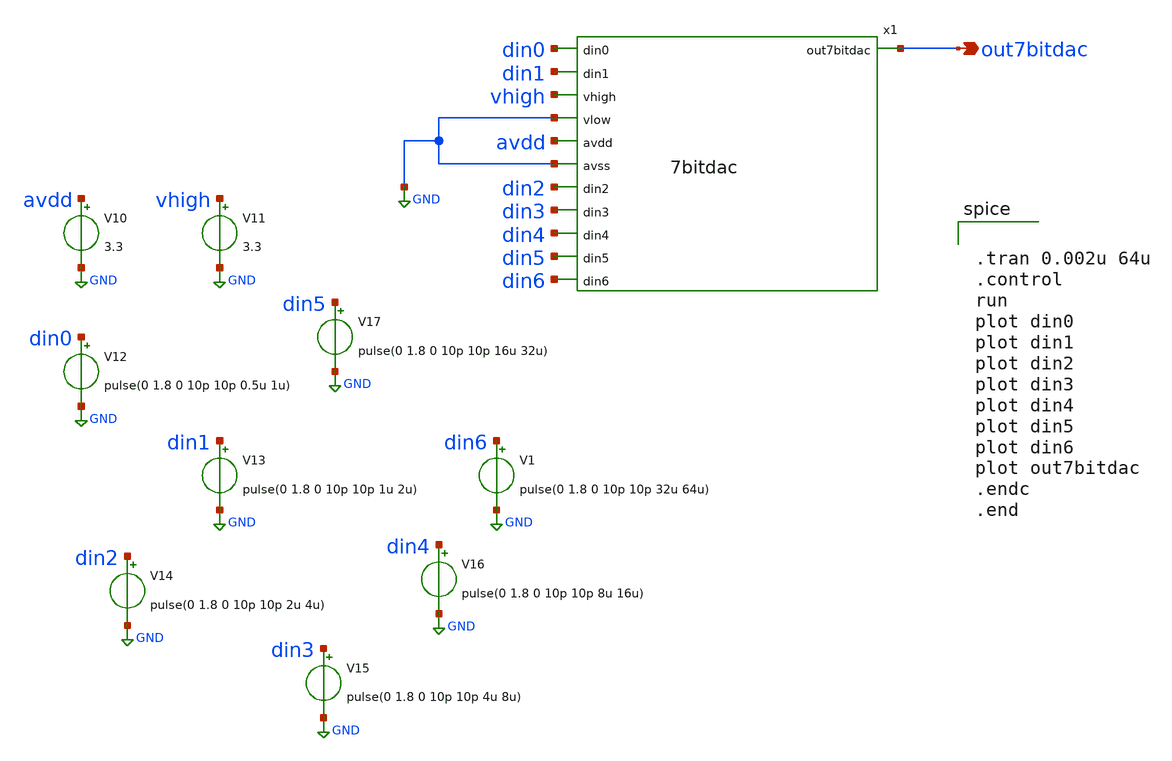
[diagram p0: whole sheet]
** sch_path: xschem/tb_7bitdac.sch
**.subckt tb_7bitdac out7bitdac
*.opin out7bitdac
x1 out7bitdac din0 din1 vhigh GND avdd GND din2 din3 din4 din5 din6 7bitdac
V10 avdd GND 3.3
V11 vhigh GND 3.3
V12 din0 GND pulse(0 1.8 0 10p 10p 0.5u 1u)
V13 din1 GND pulse(0 1.8 0 10p 10p 1u 2u)
V14 din2 GND pulse(0 1.8 0 10p 10p 2u 4u)
V15 din3 GND pulse(0 1.8 0 10p 10p 4u 8u)
V16 din4 GND pulse(0 1.8 0 10p 10p 8u 16u)
V17 din5 GND pulse(0 1.8 0 10p 10p 16u 32u)
V1 din6 GND pulse(0 1.8 0 10p 10p 32u 64u)
**** begin user architecture code

** opencircuitdesign pdks install
.lib $::SKYWATER_MODELS/sky130.lib.spice tt




.tran 0.002u 64u
.control
run
plot din0
plot din1
plot din2
plot din3
plot din4
plot din5
plot din6
plot out7bitdac
.endc
.end

**** end user architecture code
**.ends
.GLOBAL GND
.end
